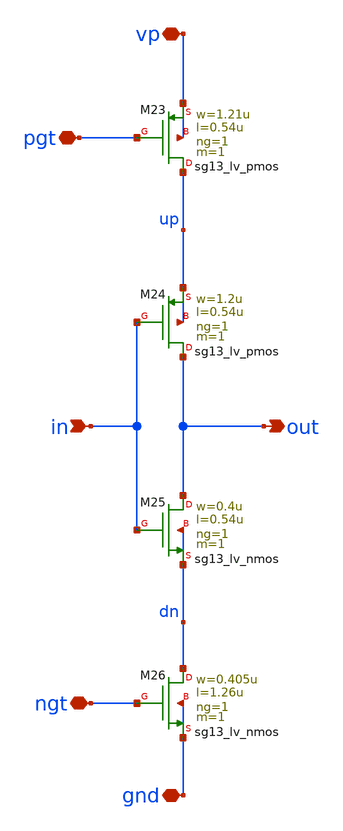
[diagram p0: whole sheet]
** sch_path: vco/vco_cell/vco_delay_cell_3BL.sch
**.subckt vco_delay_cell_3BL in out gnd vp pgt ngt
*.ipin in
*.opin out
*.iopin gnd
*.iopin vp
*.iopin pgt
*.iopin ngt
XM23 up pgt vp vp sg13_lv_pmos w=1.21u l=0.54u ng=1 m=1 mm_ok=1
XM24 out in up up sg13_lv_pmos w=1.2u l=0.54u ng=1 m=1 mm_ok=1
XM25 out in dn dn sg13_lv_nmos w=0.4u l=0.54u ng=1 m=1 mm_ok=1
XM26 dn ngt gnd gnd sg13_lv_nmos w=0.405u l=1.26u ng=1 m=1 mm_ok=1
**.ends
.end
